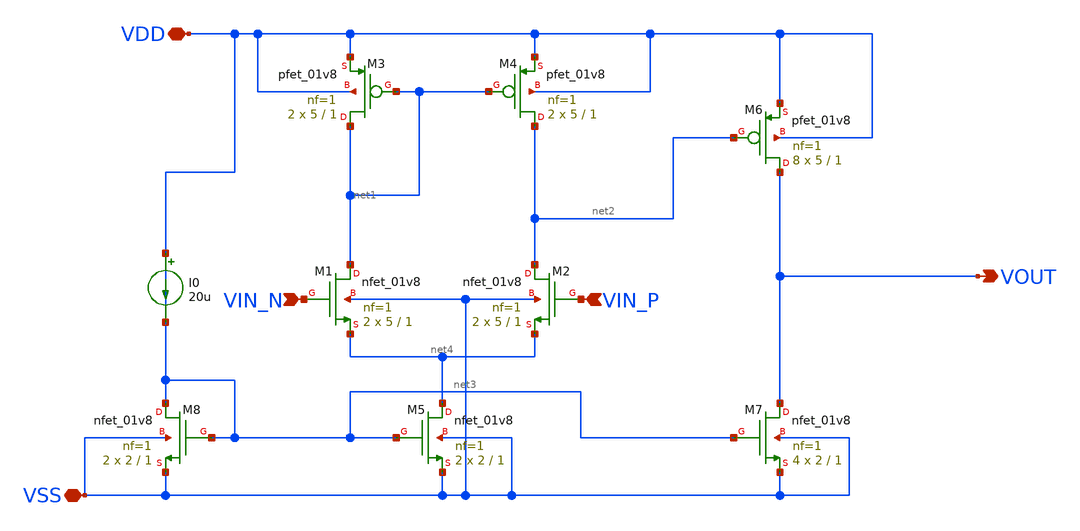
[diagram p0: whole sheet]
** sch_path: analog/bootcamp_opamp/schematics/opamp_two_stage.sch
**.subckt opamp_two_stage VIN_N VIN_P VOUT VSS VDD
*.ipin VIN_N
*.ipin VIN_P
*.opin VOUT
*.iopin VSS
*.iopin VDD
XM4 net2 net1 VDD VDD sky130_fd_pr__pfet_01v8 L=1 W=5 nf=1 ad='int((nf+1)/2) * W/nf * 0.29' as='int((nf+2)/2) * W/nf * 0.29'
+ pd='2*int((nf+1)/2) * (W/nf + 0.29)' ps='2*int((nf+2)/2) * (W/nf + 0.29)' nrd='0.29 / W' nrs='0.29 / W'
+ sa=0 sb=0 sd=0 mult=2 m=2
XM3 net1 net1 VDD VDD sky130_fd_pr__pfet_01v8 L=1 W=5 nf=1 ad='int((nf+1)/2) * W/nf * 0.29' as='int((nf+2)/2) * W/nf * 0.29'
+ pd='2*int((nf+1)/2) * (W/nf + 0.29)' ps='2*int((nf+2)/2) * (W/nf + 0.29)' nrd='0.29 / W' nrs='0.29 / W'
+ sa=0 sb=0 sd=0 mult=2 m=2
XM6 VOUT net2 VDD VDD sky130_fd_pr__pfet_01v8 L=1 W=5 nf=1 ad='int((nf+1)/2) * W/nf * 0.29' as='int((nf+2)/2) * W/nf * 0.29'
+ pd='2*int((nf+1)/2) * (W/nf + 0.29)' ps='2*int((nf+2)/2) * (W/nf + 0.29)' nrd='0.29 / W' nrs='0.29 / W'
+ sa=0 sb=0 sd=0 mult=8 m=8
XM2 net2 VIN_P net4 VSS sky130_fd_pr__nfet_01v8 L=1 W=5 nf=1 ad='int((nf+1)/2) * W/nf * 0.29' as='int((nf+2)/2) * W/nf * 0.29'
+ pd='2*int((nf+1)/2) * (W/nf + 0.29)' ps='2*int((nf+2)/2) * (W/nf + 0.29)' nrd='0.29 / W' nrs='0.29 / W'
+ sa=0 sb=0 sd=0 mult=2 m=2
XM1 net1 VIN_N net4 VSS sky130_fd_pr__nfet_01v8 L=1 W=5 nf=1 ad='int((nf+1)/2) * W/nf * 0.29' as='int((nf+2)/2) * W/nf * 0.29'
+ pd='2*int((nf+1)/2) * (W/nf + 0.29)' ps='2*int((nf+2)/2) * (W/nf + 0.29)' nrd='0.29 / W' nrs='0.29 / W'
+ sa=0 sb=0 sd=0 mult=2 m=2
XM5 net4 net3 VSS VSS sky130_fd_pr__nfet_01v8 L=1 W=2 nf=1 ad='int((nf+1)/2) * W/nf * 0.29' as='int((nf+2)/2) * W/nf * 0.29'
+ pd='2*int((nf+1)/2) * (W/nf + 0.29)' ps='2*int((nf+2)/2) * (W/nf + 0.29)' nrd='0.29 / W' nrs='0.29 / W'
+ sa=0 sb=0 sd=0 mult=2 m=2
XM7 VOUT net3 VSS VSS sky130_fd_pr__nfet_01v8 L=1 W=2 nf=1 ad='int((nf+1)/2) * W/nf * 0.29' as='int((nf+2)/2) * W/nf * 0.29'
+ pd='2*int((nf+1)/2) * (W/nf + 0.29)' ps='2*int((nf+2)/2) * (W/nf + 0.29)' nrd='0.29 / W' nrs='0.29 / W'
+ sa=0 sb=0 sd=0 mult=4 m=4
XM8 net3 net3 VSS VSS sky130_fd_pr__nfet_01v8 L=1 W=2 nf=1 ad='int((nf+1)/2) * W/nf * 0.29' as='int((nf+2)/2) * W/nf * 0.29'
+ pd='2*int((nf+1)/2) * (W/nf + 0.29)' ps='2*int((nf+2)/2) * (W/nf + 0.29)' nrd='0.29 / W' nrs='0.29 / W'
+ sa=0 sb=0 sd=0 mult=2 m=2
I0 VDD net3 20u
**.ends
.end
